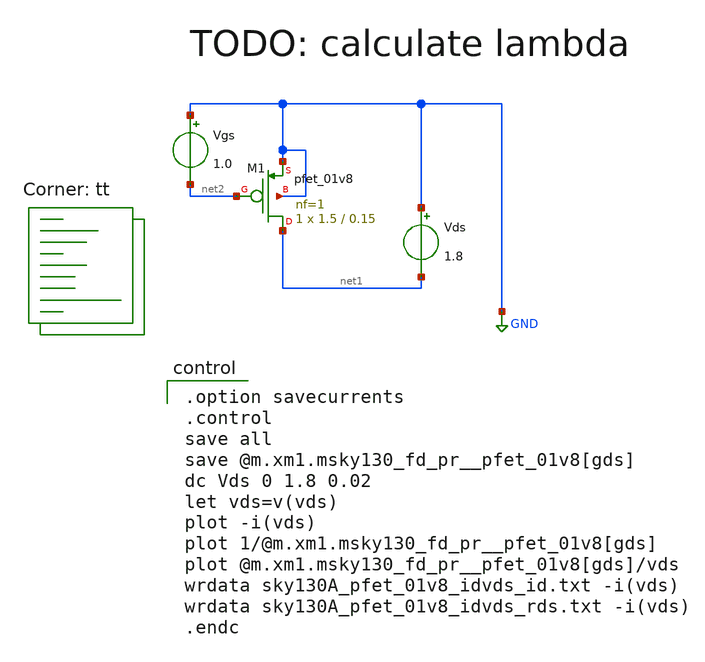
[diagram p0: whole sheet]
** sch_path: xschem/MOSFET/sky130A_pfet_01v8_idvds.sch
**.subckt sky130A_pfet_01v8_idvds
Vgs GND net2 1.0
Vds GND net1 1.8
XM1 net1 net2 GND GND sky130_fd_pr__pfet_01v8 L=0.15 W=1.5 nf=1 ad='int((nf+1)/2) * W/nf * 0.29' as='int((nf+2)/2) * W/nf * 0.29'
+ pd='2*int((nf+1)/2) * (W/nf + 0.29)' ps='2*int((nf+2)/2) * (W/nf + 0.29)' nrd='0.29 / W' nrs='0.29 / W'
+ sa=0 sb=0 sd=0 mult=1 m=1
**** begin user architecture code

.option savecurrents
.control
save all
save @m.xm1.msky130_fd_pr__pfet_01v8[gds]
dc Vds 0 1.8 0.02
let vds=v(vds)
plot -i(vds)
plot 1/@m.xm1.msky130_fd_pr__pfet_01v8[gds]
plot @m.xm1.msky130_fd_pr__pfet_01v8[gds]/vds
wrdata sky130A_pfet_01v8_idvds_id.txt -i(vds)
wrdata sky130A_pfet_01v8_idvds_rds.txt -i(vds)
.endc

.lib $::SKYWATER_MODELS/sky130.lib.spice tt
**** end user architecture code
**.ends
.GLOBAL GND
.end
